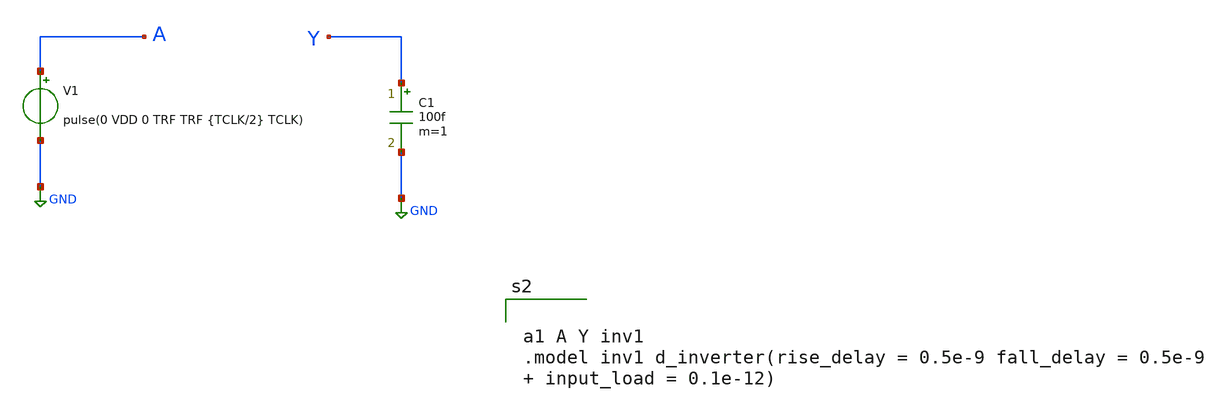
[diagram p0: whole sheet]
** sch_path: Designs/inv_tb.sch
**.subckt inv_tb
V1 A GND pulse(0 VDD 0 TRF TRF {TCLK/2} TCLK)
C1 Y GND 100f m=1
**** begin user architecture code



*These are the values of the parameters to be used
.param VDD=2 VCC=VDD
.param TRF=1n TCLK=100n
.param TSTOP={5*TCLK} TDROP=0
*Analysis setup and control statements
.tran 100p {TSTOP} {TDROP}
*save all voltages and currents
.save all
*options for an accurate precision output
.options reltol=1e-6 vntol=1u abstol=1p
* option to make output file ascii
*.options filetype=ascii




a1 A Y inv1
.model inv1 d_inverter(rise_delay = 0.5e-9 fall_delay = 0.5e-9  input_load = 0.1e-12)


**** end user architecture code
**.ends
.GLOBAL GND
.end
